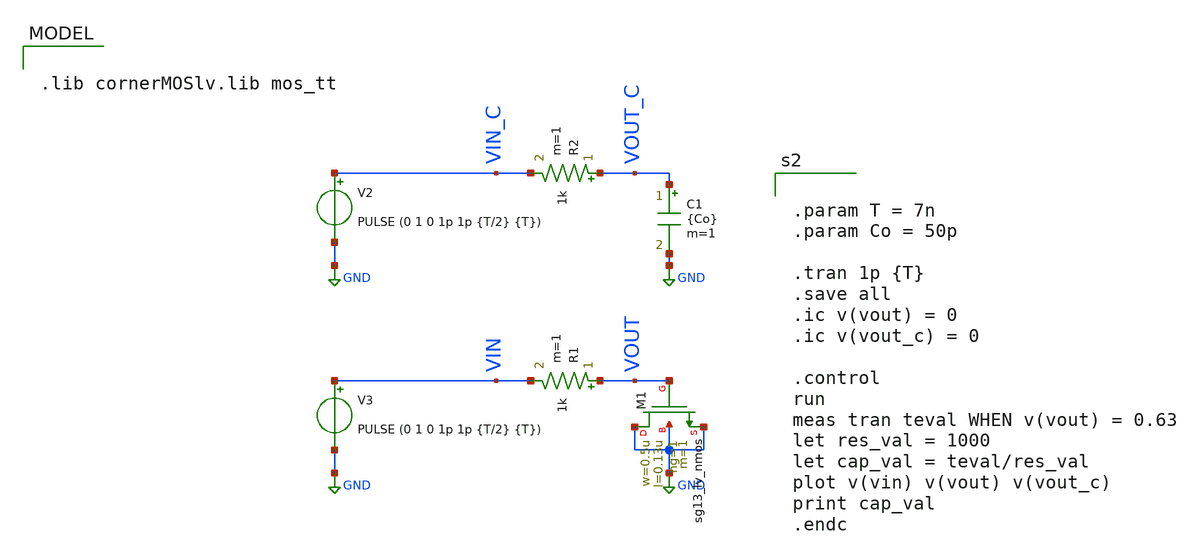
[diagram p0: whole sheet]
** sch_path: xschem/TB/TB_lvNMOS_cgate_ext.sch
**.subckt TB_lvNMOS_cgate_ext
R1 VOUT VIN 1k m=1
R2 VOUT_C VIN_C 1k m=1
V2 VIN_C GND PULSE (0 1 0 1p 1p {T/2} {T})
C1 VOUT_C GND {Co} m=1
V3 VIN GND PULSE (0 1 0 1p 1p {T/2} {T})
XM1 GND VOUT GND GND sg13_lv_nmos w=0.5u l=0.13u ng=1 m=1 mm_ok=1
**** begin user architecture code

.lib cornerMOSlv.lib mos_tt



.param T = 7n
.param Co = 50p

.tran 1p {T}
.save all
.ic v(vout) = 0
.ic v(vout_c) = 0

.control
run
meas tran teval WHEN v(vout) = 0.63
let res_val = 1000
let cap_val = teval/res_val
plot v(vin) v(vout) v(vout_c)
print cap_val
.endc




*M1 hvPMOS
.param temp=27
.param mult_M1 = 12000
.param w_M1 =10u
.param l_M1 = 0.4u
.param ng_M1 = 1

*M2 hvNMOS
.param mult_M2 = 4000
.param w_M2 =10u
.param l_M2 =0.45u
.param ng_M2 =1






**** end user architecture code
**.ends
.GLOBAL GND
.end
